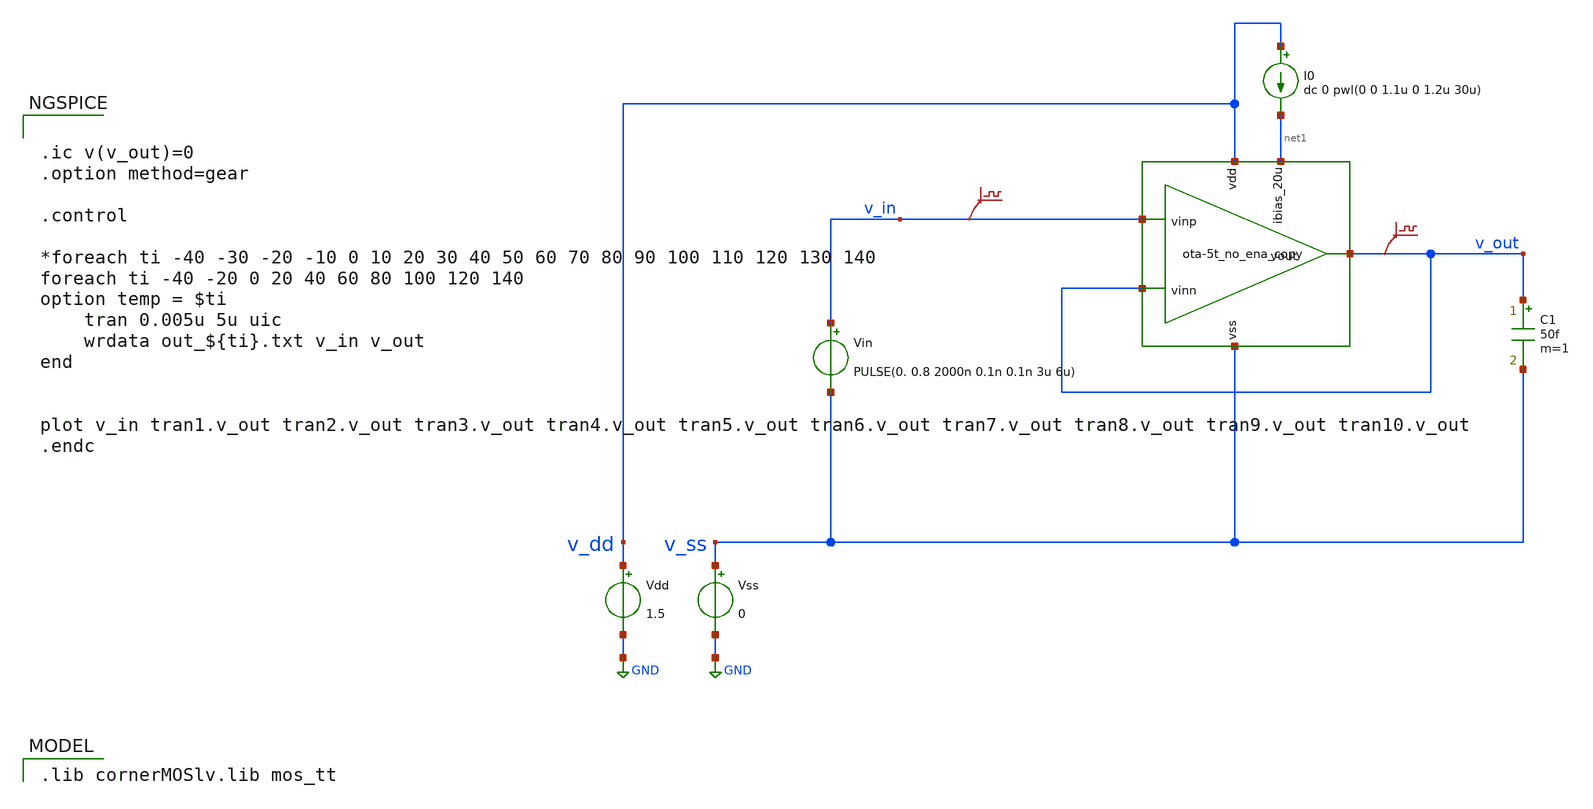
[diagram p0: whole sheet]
** sch_path: 004_Real_Circuits/004_testbench_ota_results/temperature_analysis/ota-5t_tb-tran_no_ena.sch
* (c) 2024-2025 Harald Pretl, Apache-2.0 license
**.subckt ota-5t_tb-tran_no_ena
Vdd v_dd GND 1.5
Vss v_ss GND 0
C1 v_out v_ss 50f m=1
Vin v_in v_ss PULSE(0. 0.8 2000n 0.1n 0.1n 3u 6u)
I0 v_dd net1 dc 0 pwl(0 0 1.1u 0 1.2u 30u)
.save v(v_in)
.save v(v_out)
x1 v_dd v_out v_in v_out net1 v_ss ota-5t_no_ena_copy
**** begin user architecture code
 .lib cornerMOSlv.lib mos_tt



.ic v(v_out)=0
.option method=gear

.control

*foreach ti -40 -30 -20 -10 0 10 20 30 40 50 60 70 80 90 100 110 120 130 140
foreach ti -40 -20 0 20 40 60 80 100 120 140
option temp = $ti
    tran 0.005u 5u uic
    wrdata out_${ti}.txt v_in v_out
end


plot v_in tran1.v_out tran2.v_out tran3.v_out tran4.v_out tran5.v_out tran6.v_out tran7.v_out
+ tran8.v_out tran9.v_out tran10.v_out
.endc



**** end user architecture code
**.ends

* expanding   symbol:  003_version_second_output_stage/ota-5t_no_ena_copy.sym # of pins=6
** sym_path: 004_Real_Circuits/003_version_second_output_stage/ota-5t_no_ena_copy.sym
** sch_path: 004_Real_Circuits/003_version_second_output_stage/ota-5t_no_ena_copy.sch
.subckt ota-5t_no_ena_copy vdd vout vinp vinn ibias_20u vss
*.opin vout
*.iopin vdd
*.ipin vinp
*.ipin vinn
*.ipin ibias_20u
*.iopin vss
XM5 tail ibias_20u vss vss sg13_lv_nmos w=1.5u l=5u ng=1 m=1 mm_ok=1
XM4 net1 gate_p vdd vdd sg13_lv_pmos w=3.5u l=5u ng=1 m=1 mm_ok=1
XM1 gate_p vinn tail vss sg13_lv_nmos w=2u l=5u ng=1 m=1 mm_ok=1
XM2 net1 vinp tail vss sg13_lv_nmos w=2u l=5u ng=1 m=1 mm_ok=1
XM3 gate_p gate_p vdd vdd sg13_lv_pmos w=3.5u l=5u ng=1 m=1 mm_ok=1
XM6 ibias_20u ibias_20u vss vss sg13_lv_nmos w=10u l=5u ng=5 m=1 mm_ok=1
XM7 vout net1 vdd vdd sg13_lv_pmos w=8.5u l=5u ng=1 m=1 mm_ok=1
XM8 vout ibias_20u vss vss sg13_lv_nmos w=0.75u l=5u ng=1 m=1 mm_ok=1
C2 net2 vout 795f m=1
R1 net1 net2 59k m=1
.ends

.GLOBAL GND
.end
